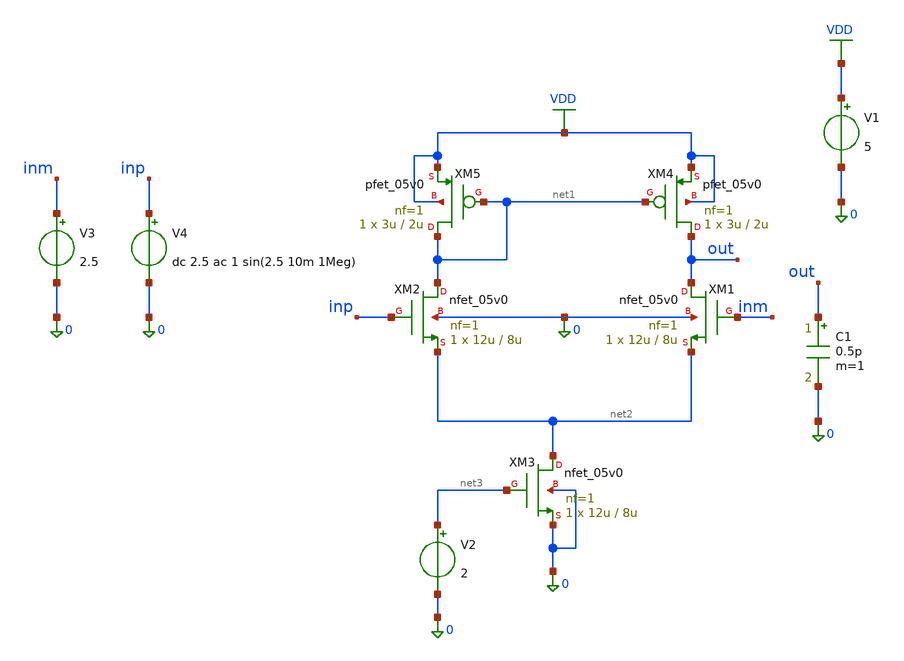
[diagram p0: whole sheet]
** sch_path: TG_gm_ff_old/gm_ff.sch
**.subckt gm_ff
XM1 out inm net2 0 nfet_05v0 L=8u W=12u nf=1 ad='int((nf+1)/2) * W/nf * 0.18u' as='int((nf+2)/2) * W/nf * 0.18u'
+ pd='2*int((nf+1)/2) * (W/nf + 0.18u)' ps='2*int((nf+2)/2) * (W/nf + 0.18u)' nrd='0.18u / W' nrs='0.18u / W'
+ sa=0 sb=0 sd=0 m=1
XM2 net1 inp net2 0 nfet_05v0 L=8u W=12u nf=1 ad='int((nf+1)/2) * W/nf * 0.18u' as='int((nf+2)/2) * W/nf * 0.18u'
+ pd='2*int((nf+1)/2) * (W/nf + 0.18u)' ps='2*int((nf+2)/2) * (W/nf + 0.18u)' nrd='0.18u / W' nrs='0.18u / W'
+ sa=0 sb=0 sd=0 m=1
XM3 net2 net3 0 0 nfet_05v0 L=8u W=12u nf=1 ad='int((nf+1)/2) * W/nf * 0.18u' as='int((nf+2)/2) * W/nf * 0.18u'
+ pd='2*int((nf+1)/2) * (W/nf + 0.18u)' ps='2*int((nf+2)/2) * (W/nf + 0.18u)' nrd='0.18u / W' nrs='0.18u / W'
+ sa=0 sb=0 sd=0 m=1
XM4 out net1 VDD VDD pfet_05v0 L=2u W=3u nf=1 ad='int((nf+1)/2) * W/nf * 0.18u' as='int((nf+2)/2) * W/nf * 0.18u'
+ pd='2*int((nf+1)/2) * (W/nf + 0.18u)' ps='2*int((nf+2)/2) * (W/nf + 0.18u)' nrd='0.18u / W' nrs='0.18u / W'
+ sa=0 sb=0 sd=0 m=1
XM5 net1 net1 VDD VDD pfet_05v0 L=2u W=3u nf=1 ad='int((nf+1)/2) * W/nf * 0.18u' as='int((nf+2)/2) * W/nf * 0.18u'
+ pd='2*int((nf+1)/2) * (W/nf + 0.18u)' ps='2*int((nf+2)/2) * (W/nf + 0.18u)' nrd='0.18u / W' nrs='0.18u / W'
+ sa=0 sb=0 sd=0 m=1
V1 VDD 0 5
V3 inm 0 2.5
V4 inp 0 dc 2.5 ac 1 sin(2.5 10m 1Meg)
C1 out 0 0.5p m=1
V2 net3 0 2
**.ends
.GLOBAL VDD
.end
